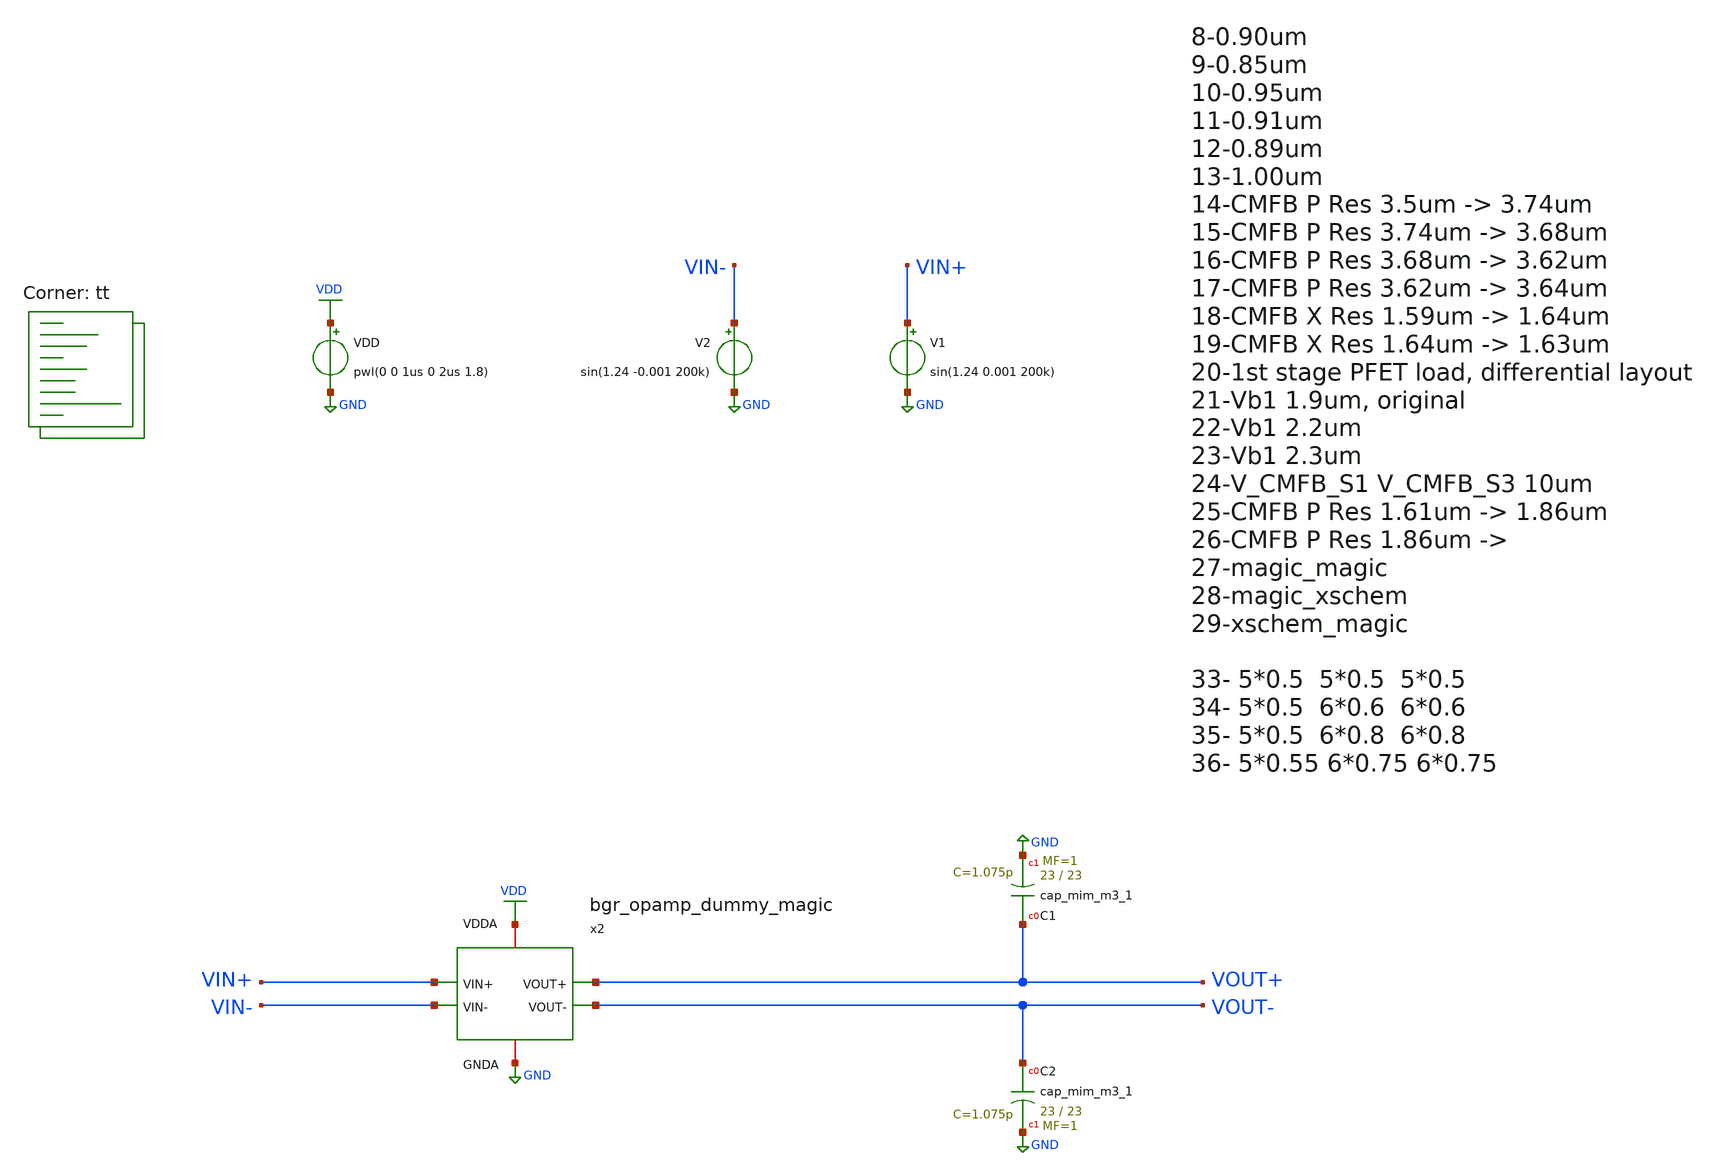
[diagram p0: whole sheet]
** sch_path: projects/opamp/xschem_ngspice/tb_bgr_opamp_dummy_magic_2.sch
**.subckt tb_bgr_opamp_dummy_magic_2
VDD VDD GND pwl(0 0 1us 0 2us 1.8)
V2 VIN- GND sin(1.24 -0.001 200k)
V1 VIN+ GND sin(1.24 0.001 200k)
XC1 VOUT+ GND sky130_fd_pr__cap_mim_m3_1 W=23 L=23 MF=1 m=1
XC2 VOUT- GND sky130_fd_pr__cap_mim_m3_1 W=23 L=23 MF=1 m=1
x2 VDD GND VOUT+ VOUT- VIN+ VIN- bgr_opamp_dummy_magic
**** begin user architecture code
.lib $::SKYWATER_MODELS/sky130.lib.spice tt




.include /foss/designs/my_design/projects/opamp/xschem_ngspice/bgr_opamp_dummy_magic.spice
* .include /foss/designs/my_design/projects/opamp/xschem_ngspice/two_stage_opamp_dummy_magic.spice
* .include /foss/designs/my_design/projects/opamp/xschem_ngspice/ref_volt_cur_gen_dummy_magic.spice


.option method=gear
.option wnflag=1
.option savecurrents

.save v(vout+) v(vout-) v(vin+) v(vin-) v(x2.two_stage_opamp_dummy_magic_0.v_cmfb_s1.t0) v(x2.two_stage_opamp_dummy_magic_0.v_cmfb_s2.t0) v(x2.two_stage_opamp_dummy_magic_0.v_cmfb_s3.t0) v(x2.two_stage_opamp_dummy_magic_0.v_cmfb_s4.t0) v(x2.two_stage_opamp_dummy_magic_0.x.t0) v(x2.two_stage_opamp_dummy_magic_0.y.t0) v(x2.two_stage_opamp_dummy_magic_0.v_tot.t0) v(x2.two_stage_opamp_dummy_magic_0.v_err_amp_ref.t0)


* .ic v(v_top) = 1.8

.control

  * let runs=3
  * let run=1

  * dowhile run <= runs
    * save v(vout+) v(vout-) v(vin+) v(vin-) v(v_err_amp_ref) v(x2.x) v(x2.y) v(x2.vb1) v(x2.vb2)
+ v(x2.vb3) v(x2.v_tot)
    save all
    remzerovec
    set appendwrite
    * dc temp -40 120 10 VDD 0 4.0 0.2
    * dc VDD 0 2.0 0.02 temp -40 120 40
    * dc V5 0 0.01 0.0001
    tran 2n 11u
    * tran 10n 150u
    * tran 1p 3n
    * tran 0.1ns 30us
    * ac dec 40 1 10T
    * write tb_bgr_opamp_dummy_magic.raw
    * write tb_bgr_opamp_dummy_magic_2.raw
    * write tb_bgr_opamp_dummy_magic_3.raw
    * write tb_bgr_opamp_dummy_magic_4.raw
    * write tb_bgr_opamp_dummy_magic_5.raw
    * write tb_bgr_opamp_dummy_magic_6.raw
    * write tb_bgr_opamp_dummy_magic_7.raw
    * write tb_bgr_opamp_dummy_magic_8.raw
    * write tb_bgr_opamp_dummy_magic_9.raw
    * write tb_bgr_opamp_dummy_magic_10.raw
    * write tb_bgr_opamp_dummy_magic_11.raw
    * write tb_bgr_opamp_dummy_magic_12.raw
    * write tb_bgr_opamp_dummy_magic_13.raw
    * write tb_bgr_opamp_dummy_magic_14.raw
    * write tb_bgr_opamp_dummy_magic_15.raw
    * write tb_bgr_opamp_dummy_magic_16.raw
    * write tb_bgr_opamp_dummy_magic_17.raw
    * write tb_bgr_opamp_dummy_magic_18.raw
    * write tb_bgr_opamp_dummy_magic_19.raw
    * write tb_bgr_opamp_dummy_magic_20.raw
    * write tb_bgr_opamp_dummy_magic_21.raw
    * write tb_bgr_opamp_dummy_magic_22.raw
    * write tb_bgr_opamp_dummy_magic_23.raw
    * write tb_bgr_opamp_dummy_magic_24.raw
    * write tb_bgr_opamp_dummy_magic_25.raw
    * write tb_bgr_opamp_dummy_magic_26.raw
    * write tb_bgr_opamp_dummy_magic_27.raw
    * write tb_bgr_opamp_dummy_magic_28.raw
    * write tb_bgr_opamp_dummy_magic_29.raw
    * write tb_bgr_opamp_dummy_magic_30.raw
    * write tb_bgr_opamp_dummy_magic_31.raw
    * write tb_bgr_opamp_dummy_magic_32.raw
    * write tb_bgr_opamp_dummy_magic_33.raw
    * write tb_bgr_opamp_dummy_magic_34.raw
    * write tb_bgr_opamp_dummy_magic_35.raw
    * write tb_bgr_opamp_dummy_magic_36.raw
    * write tb_bgr_opamp_dummy_magic_37.raw
    * write tb_bgr_opamp_dummy_magic_38.raw
    * write tb_bgr_opamp_dummy_magic_39.raw
    * write tb_bgr_opamp_dummy_magic_40.raw
    * write tb_bgr_opamp_dummy_magic_41.raw
    * write tb_bgr_opamp_dummy_magic_42.raw
    * write tb_bgr_opamp_dummy_magic_43.raw
    * write tb_bgr_opamp_dummy_magic_44.raw
    * write tb_bgr_opamp_dummy_magic_45.raw
    * write tb_bgr_opamp_dummy_magic_46.raw
    * write tb_bgr_opamp_dummy_magic_47.raw
    * write tb_bgr_opamp_dummy_magic_48.raw
    * write tb_bgr_opamp_dummy_magic_49.raw
    * write tb_bgr_opamp_dummy_magic_50.raw
    * write tb_bgr_opamp_dummy_magic_51.raw
    * write tb_bgr_opamp_dummy_magic_52.raw
    * write tb_bgr_opamp_dummy_magic_53.raw
    * write tb_bgr_opamp_dummy_magic_54.raw
    * write tb_bgr_opamp_dummy_magic_55.raw
    * write tb_bgr_opamp_dummy_magic_56.raw
    * write tb_bgr_opamp_dummy_magic_57.raw
    * write tb_bgr_opamp_dummy_magic_58.raw
    * write tb_bgr_opamp_dummy_magic_59.raw
    * write tb_bgr_opamp_dummy_magic_60.raw
    * write tb_bgr_opamp_dummy_magic_61.raw
    * write tb_bgr_opamp_dummy_magic_62.raw
    * write tb_bgr_opamp_dummy_magic_63.raw
    * write tb_bgr_opamp_dummy_magic_64.raw
    * write tb_bgr_opamp_dummy_magic_65.raw
    * write tb_bgr_opamp_dummy_magic_66.raw
    * write tb_bgr_opamp_dummy_magic_67.raw
    * write tb_bgr_opamp_dummy_magic_68.raw
    * write tb_bgr_opamp_dummy_magic_69.raw
    * write tb_bgr_opamp_dummy_magic_70.raw
    * write tb_bgr_opamp_dummy_magic_71.raw
    * write tb_bgr_opamp_dummy_magic_72.raw
    * write tb_bgr_opamp_dummy_magic_73.raw
    * write tb_bgr_opamp_dummy_magic_74.raw
    * write tb_bgr_opamp_dummy_magic_75.raw
    * write tb_bgr_opamp_dummy_magic_76.raw
    * write tb_bgr_opamp_dummy_magic_77.raw
    * write tb_bgr_opamp_dummy_magic_78.raw
    * write tb_bgr_opamp_dummy_magic_79.raw
    * write tb_bgr_opamp_dummy_magic_80.raw
    * write tb_bgr_opamp_dummy_magic_81.raw
    * write tb_bgr_opamp_dummy_magic_82.raw
    write tb_bgr_opamp_dummy_magic_83.raw
    * write tb_bgr_opamp_dummy_magic_mc.raw
    * write tb_bgr_opamp_dummy_magic_tt_mm.raw
    * write tb_bgr_opamp_dummy_magic_AC.raw
    * reset
    * let run = run + 1
  * end
.endc




**** end user architecture code
**.ends
.GLOBAL GND
.GLOBAL VDD
.end
